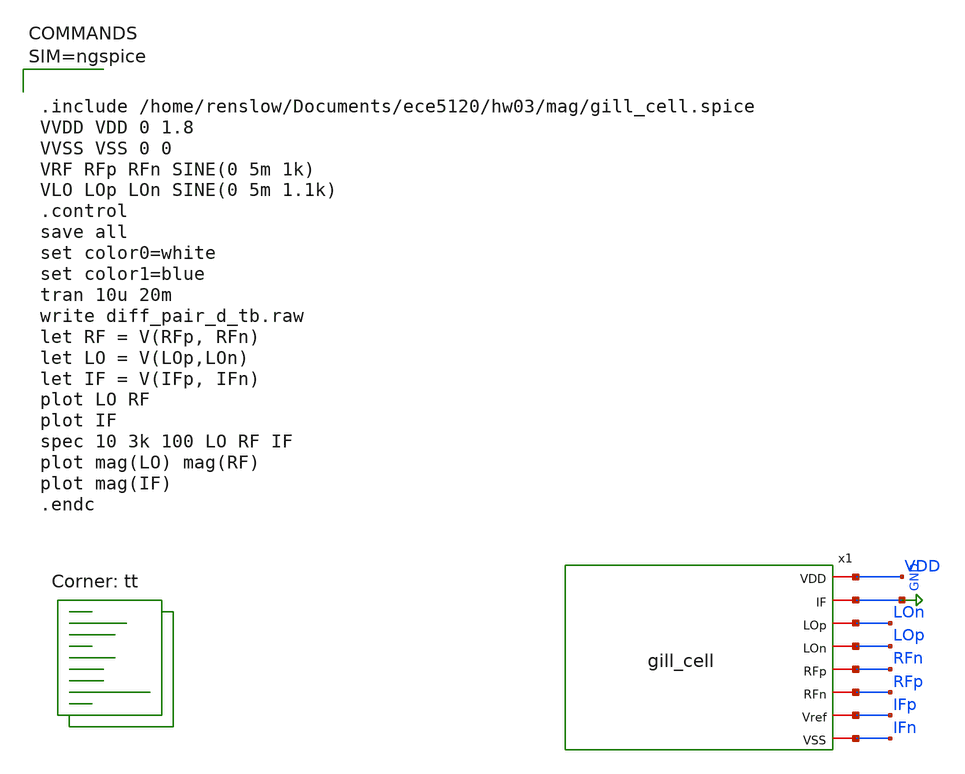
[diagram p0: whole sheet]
** sch_path: hw07/mag/gilbert_tb.sch
**.subckt gilbert_tb
x1 VDD GND LOn LOp RFn RFp IFp IFn gill_cell
**** begin user architecture code
.lib $::SKYWATER_MODELS/sky130.lib.spice tt



.include /home/renslow/Documents/ece5120/hw03/mag/gill_cell.spice
VVDD VDD 0 1.8
VVSS VSS 0 0
VRF RFp RFn SINE(0 5m 1k)
VLO LOp LOn SINE(0 5m 1.1k)
.control
save all
set color0=white
set color1=blue
tran 10u 20m
write diff_pair_d_tb.raw
let RF = V(RFp, RFn)
let LO = V(LOp,LOn)
let IF = V(IFp, IFn)
plot LO RF
plot IF
spec 10 3k 100 LO RF IF
plot mag(LO) mag(RF)
plot mag(IF)
.endc



**** end user architecture code
**.ends

* expanding   symbol:  gill_cell.sym # of pins=8
** sym_path: Project/xschem/gill_cell.sym
** sch_path: Project/xschem/gill_cell.sch
.subckt gill_cell VDD IF LOp LOn RFp RFn Vref VSS
*.iopin LOp
*.iopin LOn
*.iopin RFp
*.iopin RFn
*.iopin VDD
*.iopin VSS
*.iopin Vref
*.iopin IF
XR1 IF++ VDD VSS sky130_fd_pr__res_xhigh_po_0p69 L=6.9 mult=1 m=1
XR3 IF-- VDD VSS sky130_fd_pr__res_xhigh_po_0p69 L=6.9 mult=1 m=1
XR10 VDD LOp VSS sky130_fd_pr__res_xhigh_po_0p69 L=1.38 mult=1 m=1
XR11 LOp VSS VSS sky130_fd_pr__res_xhigh_po_0p69 L=3.45 mult=1 m=1
XR12 LOn VDD VSS sky130_fd_pr__res_xhigh_po_0p69 L=1.38 mult=1 m=1
XR13 VSS LOn VSS sky130_fd_pr__res_xhigh_po_0p69 L=3.45 mult=1 m=1
XM2 net1 VM VSS VSS sky130_fd_pr__nfet_01v8 L=1.1 W=40 nf=1 ad='int((nf+1)/2) * W/nf * 0.29' as='int((nf+2)/2) * W/nf * 0.29'
+ pd='2*int((nf+1)/2) * (W/nf + 0.29)' ps='2*int((nf+2)/2) * (W/nf + 0.29)' nrd='0.29 / W' nrs='0.29 / W'
+ sa=0 sb=0 sd=0 mult=1 m=1
XM3 Vmid RFp net1 VSS sky130_fd_pr__nfet_01v8 L=1.1 W=40 nf=1 ad='int((nf+1)/2) * W/nf * 0.29' as='int((nf+2)/2) * W/nf * 0.29'
+ pd='2*int((nf+1)/2) * (W/nf + 0.29)' ps='2*int((nf+2)/2) * (W/nf + 0.29)' nrd='0.29 / W' nrs='0.29 / W'
+ sa=0 sb=0 sd=0 mult=1 m=1
XM5 IF++ LOp Vmid VSS sky130_fd_pr__nfet_01v8 L=1.1 W=40 nf=1 ad='int((nf+1)/2) * W/nf * 0.29' as='int((nf+2)/2) * W/nf * 0.29'
+ pd='2*int((nf+1)/2) * (W/nf + 0.29)' ps='2*int((nf+2)/2) * (W/nf + 0.29)' nrd='0.29 / W' nrs='0.29 / W'
+ sa=0 sb=0 sd=0 mult=1 m=1
XM7 IF++ LOn Vmid2 VSS sky130_fd_pr__nfet_01v8 L=1.1 W=40 nf=1 ad='int((nf+1)/2) * W/nf * 0.29' as='int((nf+2)/2) * W/nf * 0.29'
+ pd='2*int((nf+1)/2) * (W/nf + 0.29)' ps='2*int((nf+2)/2) * (W/nf + 0.29)' nrd='0.29 / W' nrs='0.29 / W'
+ sa=0 sb=0 sd=0 mult=1 m=1
XM4 Vmid2 RFn net1 VSS sky130_fd_pr__nfet_01v8 L=1.1 W=40 nf=1 ad='int((nf+1)/2) * W/nf * 0.29' as='int((nf+2)/2) * W/nf * 0.29'
+ pd='2*int((nf+1)/2) * (W/nf + 0.29)' ps='2*int((nf+2)/2) * (W/nf + 0.29)' nrd='0.29 / W' nrs='0.29 / W'
+ sa=0 sb=0 sd=0 mult=1 m=1
XM8 IF-- LOp Vmid2 VSS sky130_fd_pr__nfet_01v8 L=1.1 W=40 nf=1 ad='int((nf+1)/2) * W/nf * 0.29' as='int((nf+2)/2) * W/nf * 0.29'
+ pd='2*int((nf+1)/2) * (W/nf + 0.29)' ps='2*int((nf+2)/2) * (W/nf + 0.29)' nrd='0.29 / W' nrs='0.29 / W'
+ sa=0 sb=0 sd=0 mult=1 m=1
XM6 IF-- LOn Vmid VSS sky130_fd_pr__nfet_01v8 L=1.1 W=40 nf=1 ad='int((nf+1)/2) * W/nf * 0.29' as='int((nf+2)/2) * W/nf * 0.29'
+ pd='2*int((nf+1)/2) * (W/nf + 0.29)' ps='2*int((nf+2)/2) * (W/nf + 0.29)' nrd='0.29 / W' nrs='0.29 / W'
+ sa=0 sb=0 sd=0 mult=1 m=1
XM9 Vamp VM VSS VSS sky130_fd_pr__nfet_01v8 L=1.1 W=40 nf=1 ad='int((nf+1)/2) * W/nf * 0.29' as='int((nf+2)/2) * W/nf * 0.29'
+ pd='2*int((nf+1)/2) * (W/nf + 0.29)' ps='2*int((nf+2)/2) * (W/nf + 0.29)' nrd='0.29 / W' nrs='0.29 / W'
+ sa=0 sb=0 sd=0 mult=1 m=1
XM10 IFn IF++ Vamp VSS sky130_fd_pr__nfet_01v8 L=1.1 W=40 nf=1 ad='int((nf+1)/2) * W/nf * 0.29' as='int((nf+2)/2) * W/nf * 0.29'
+ pd='2*int((nf+1)/2) * (W/nf + 0.29)' ps='2*int((nf+2)/2) * (W/nf + 0.29)' nrd='0.29 / W' nrs='0.29 / W'
+ sa=0 sb=0 sd=0 mult=1 m=1
XM11 IFp IF-- Vamp VSS sky130_fd_pr__nfet_01v8 L=1.1 W=40 nf=1 ad='int((nf+1)/2) * W/nf * 0.29' as='int((nf+2)/2) * W/nf * 0.29'
+ pd='2*int((nf+1)/2) * (W/nf + 0.29)' ps='2*int((nf+2)/2) * (W/nf + 0.29)' nrd='0.29 / W' nrs='0.29 / W'
+ sa=0 sb=0 sd=0 mult=1 m=1
XR14 IFp VDD VSS sky130_fd_pr__res_xhigh_po_0p69 L=9.67 mult=1 m=1
XR15 IFn VDD VSS sky130_fd_pr__res_xhigh_po_0p69 L=9.67 mult=1 m=1
XM1 net2 Vref VSS VSS sky130_fd_pr__nfet_01v8 L=2 W=5 nf=1 ad='int((nf+1)/2) * W/nf * 0.29' as='int((nf+2)/2) * W/nf * 0.29'
+ pd='2*int((nf+1)/2) * (W/nf + 0.29)' ps='2*int((nf+2)/2) * (W/nf + 0.29)' nrd='0.29 / W' nrs='0.29 / W'
+ sa=0 sb=0 sd=0 mult=1 m=1
XM12 VM VM VSS VSS sky130_fd_pr__nfet_01v8 L=2 W=10 nf=1 ad='int((nf+1)/2) * W/nf * 0.29' as='int((nf+2)/2) * W/nf * 0.29'
+ pd='2*int((nf+1)/2) * (W/nf + 0.29)' ps='2*int((nf+2)/2) * (W/nf + 0.29)' nrd='0.29 / W' nrs='0.29 / W'
+ sa=0 sb=0 sd=0 mult=1 m=1
XM15 VM net2 VDD VDD sky130_fd_pr__pfet_01v8 L=8 W=5 nf=1 ad='int((nf+1)/2) * W/nf * 0.29' as='int((nf+2)/2) * W/nf * 0.29'
+ pd='2*int((nf+1)/2) * (W/nf + 0.29)' ps='2*int((nf+2)/2) * (W/nf + 0.29)' nrd='0.29 / W' nrs='0.29 / W'
+ sa=0 sb=0 sd=0 mult=1 m=1
XM13 net2 net2 VDD VDD sky130_fd_pr__pfet_01v8 L=8 W=5 nf=1 ad='int((nf+1)/2) * W/nf * 0.29' as='int((nf+2)/2) * W/nf * 0.29'
+ pd='2*int((nf+1)/2) * (W/nf + 0.29)' ps='2*int((nf+2)/2) * (W/nf + 0.29)' nrd='0.29 / W' nrs='0.29 / W'
+ sa=0 sb=0 sd=0 mult=1 m=1
XM14 IF IFp VSS VSS sky130_fd_pr__nfet_01v8 L=1 W=40 nf=1 ad='int((nf+1)/2) * W/nf * 0.29' as='int((nf+2)/2) * W/nf * 0.29'
+ pd='2*int((nf+1)/2) * (W/nf + 0.29)' ps='2*int((nf+2)/2) * (W/nf + 0.29)' nrd='0.29 / W' nrs='0.29 / W'
+ sa=0 sb=0 sd=0 mult=1 m=1
XM16 VDD Vref IF VSS sky130_fd_pr__nfet_01v8 L=1 W=40 nf=1 ad='int((nf+1)/2) * W/nf * 0.29' as='int((nf+2)/2) * W/nf * 0.29'
+ pd='2*int((nf+1)/2) * (W/nf + 0.29)' ps='2*int((nf+2)/2) * (W/nf + 0.29)' nrd='0.29 / W' nrs='0.29 / W'
+ sa=0 sb=0 sd=0 mult=1 m=1
.ends

.GLOBAL GND
.end
